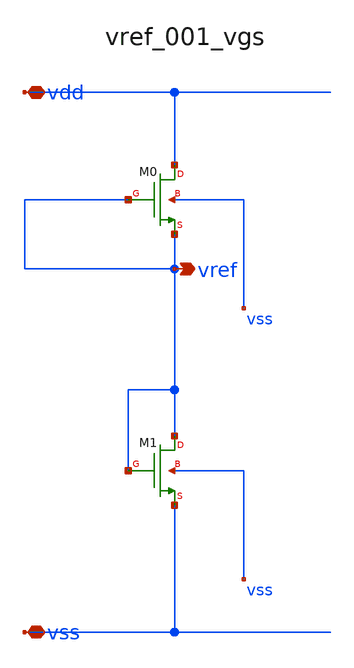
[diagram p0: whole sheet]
** sch_path: analog-db/raw/vref_001_vgs/vref_001_vgs.sch
**.subckt vref_001_vgs vdd vss vref
*.iopin vdd
*.iopin vss
*.opin vref
XM0 vdd vref vref vss sg13_lv_nmos w=x_dut_xm0_w l=x_dut_xm0_l ng=1 m=x_dut_xm0_m
XM1 vref vref vss vss sg13_hv_nmos w=x_dut_xm1_w l=x_dut_xm1_l ng=1 m=x_dut_xm1_m
**.ends
.end
